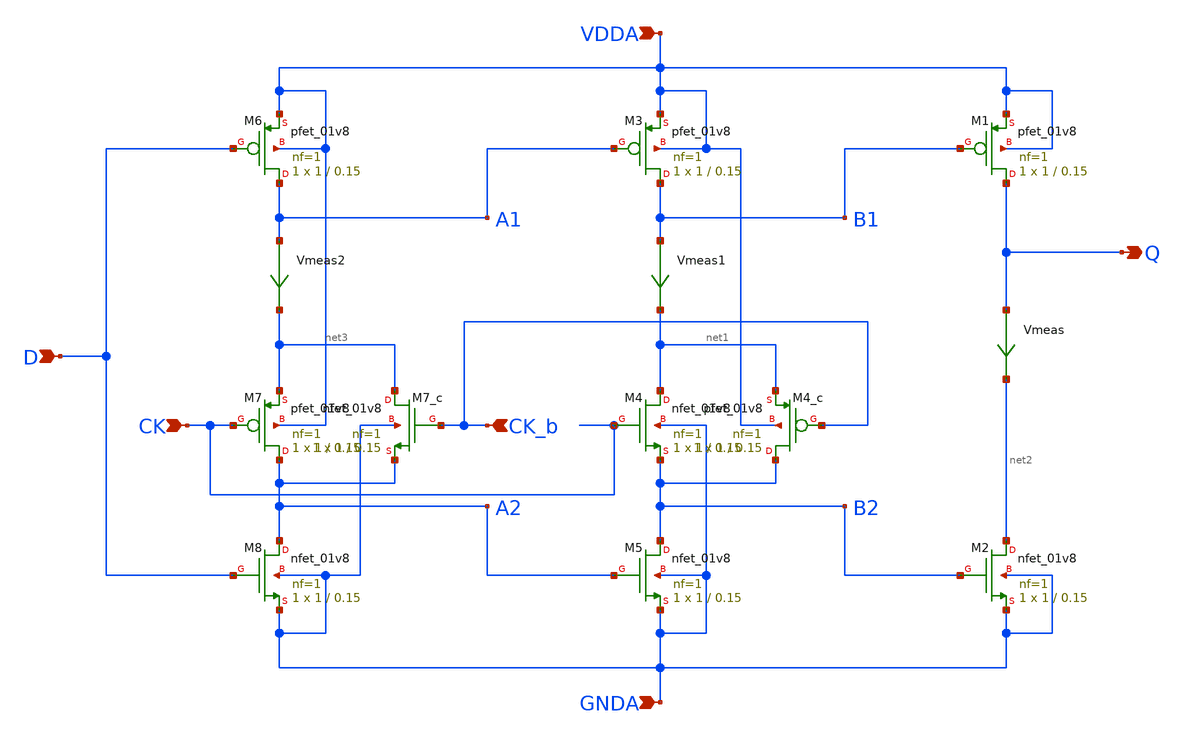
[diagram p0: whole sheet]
** sch_path: projects/pll/divider/xschem_ngspice/TSPC_FF_comp_sw.sch
**.subckt TSPC_FF_comp_sw CK D Q VDDA GNDA CK_b
*.ipin CK
*.ipin D
*.opin Q
*.ipin VDDA
*.ipin GNDA
*.ipin CK_b
XM1 Q B1 VDDA VDDA sky130_fd_pr__pfet_01v8 L=0.15 W=1 nf=1 ad='int((nf+1)/2) * W/nf * 0.29' as='int((nf+2)/2) * W/nf * 0.29'
+ pd='2*int((nf+1)/2) * (W/nf + 0.29)' ps='2*int((nf+2)/2) * (W/nf + 0.29)' nrd='0.29 / W' nrs='0.29 / W'
+ sa=0 sb=0 sd=0 mult=1 m=1
XM4 net1 CK B2 GNDA sky130_fd_pr__nfet_01v8 L=0.15 W=1 nf=1 ad='int((nf+1)/2) * W/nf * 0.29' as='int((nf+2)/2) * W/nf * 0.29'
+ pd='2*int((nf+1)/2) * (W/nf + 0.29)' ps='2*int((nf+2)/2) * (W/nf + 0.29)' nrd='0.29 / W' nrs='0.29 / W'
+ sa=0 sb=0 sd=0 mult=1 m=1
Vmeas Q net2 0
.save i(vmeas)
XM2 net2 B2 GNDA GNDA sky130_fd_pr__nfet_01v8 L=0.15 W=1 nf=1 ad='int((nf+1)/2) * W/nf * 0.29' as='int((nf+2)/2) * W/nf * 0.29'
+ pd='2*int((nf+1)/2) * (W/nf + 0.29)' ps='2*int((nf+2)/2) * (W/nf + 0.29)' nrd='0.29 / W' nrs='0.29 / W'
+ sa=0 sb=0 sd=0 mult=1 m=1
XM3 B1 A1 VDDA VDDA sky130_fd_pr__pfet_01v8 L=0.15 W=1 nf=1 ad='int((nf+1)/2) * W/nf * 0.29' as='int((nf+2)/2) * W/nf * 0.29'
+ pd='2*int((nf+1)/2) * (W/nf + 0.29)' ps='2*int((nf+2)/2) * (W/nf + 0.29)' nrd='0.29 / W' nrs='0.29 / W'
+ sa=0 sb=0 sd=0 mult=1 m=1
XM5 B2 A2 GNDA GNDA sky130_fd_pr__nfet_01v8 L=0.15 W=1 nf=1 ad='int((nf+1)/2) * W/nf * 0.29' as='int((nf+2)/2) * W/nf * 0.29'
+ pd='2*int((nf+1)/2) * (W/nf + 0.29)' ps='2*int((nf+2)/2) * (W/nf + 0.29)' nrd='0.29 / W' nrs='0.29 / W'
+ sa=0 sb=0 sd=0 mult=1 m=1
Vmeas1 B1 net1 0
.save i(vmeas1)
XM6 A1 D VDDA VDDA sky130_fd_pr__pfet_01v8 L=0.15 W=1 nf=1 ad='int((nf+1)/2) * W/nf * 0.29' as='int((nf+2)/2) * W/nf * 0.29'
+ pd='2*int((nf+1)/2) * (W/nf + 0.29)' ps='2*int((nf+2)/2) * (W/nf + 0.29)' nrd='0.29 / W' nrs='0.29 / W'
+ sa=0 sb=0 sd=0 mult=1 m=1
XM8 A2 D GNDA GNDA sky130_fd_pr__nfet_01v8 L=0.15 W=1 nf=1 ad='int((nf+1)/2) * W/nf * 0.29' as='int((nf+2)/2) * W/nf * 0.29'
+ pd='2*int((nf+1)/2) * (W/nf + 0.29)' ps='2*int((nf+2)/2) * (W/nf + 0.29)' nrd='0.29 / W' nrs='0.29 / W'
+ sa=0 sb=0 sd=0 mult=1 m=1
Vmeas2 A1 net3 0
.save i(vmeas2)
XM7 A2 CK net3 VDDA sky130_fd_pr__pfet_01v8 L=0.15 W=1 nf=1 ad='int((nf+1)/2) * W/nf * 0.29' as='int((nf+2)/2) * W/nf * 0.29'
+ pd='2*int((nf+1)/2) * (W/nf + 0.29)' ps='2*int((nf+2)/2) * (W/nf + 0.29)' nrd='0.29 / W' nrs='0.29 / W'
+ sa=0 sb=0 sd=0 mult=1 m=1
XM4_c B2 CK_b net1 VDDA sky130_fd_pr__pfet_01v8 L=0.15 W=1 nf=1 ad='int((nf+1)/2) * W/nf * 0.29' as='int((nf+2)/2) * W/nf * 0.29'
+ pd='2*int((nf+1)/2) * (W/nf + 0.29)' ps='2*int((nf+2)/2) * (W/nf + 0.29)' nrd='0.29 / W' nrs='0.29 / W'
+ sa=0 sb=0 sd=0 mult=1 m=1
XM7_c net3 CK_b A2 GNDA sky130_fd_pr__nfet_01v8 L=0.15 W=1 nf=1 ad='int((nf+1)/2) * W/nf * 0.29' as='int((nf+2)/2) * W/nf * 0.29'
+ pd='2*int((nf+1)/2) * (W/nf + 0.29)' ps='2*int((nf+2)/2) * (W/nf + 0.29)' nrd='0.29 / W' nrs='0.29 / W'
+ sa=0 sb=0 sd=0 mult=1 m=1
**.ends
.end
